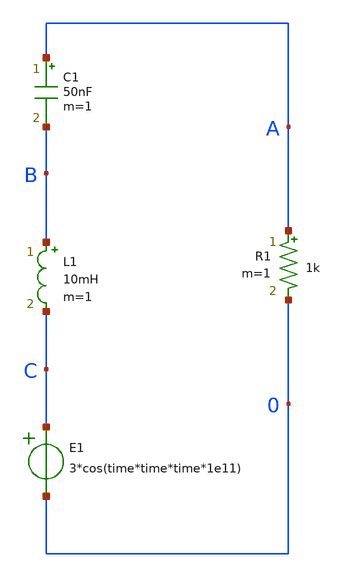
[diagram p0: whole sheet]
** sch_path: Bai1_Basic_RLC.sch
**.subckt Bai1_Basic_RLC
C1 A B 50nF m=1
R1 A 0 1k m=1
E1 C 0 VOL=' 3*cos(time*time*time*1e11) '
L1 B C 10mH m=1
**** begin user architecture code

.tran 10n 2000u uic
.save all

**** end user architecture code
**.ends
.end
